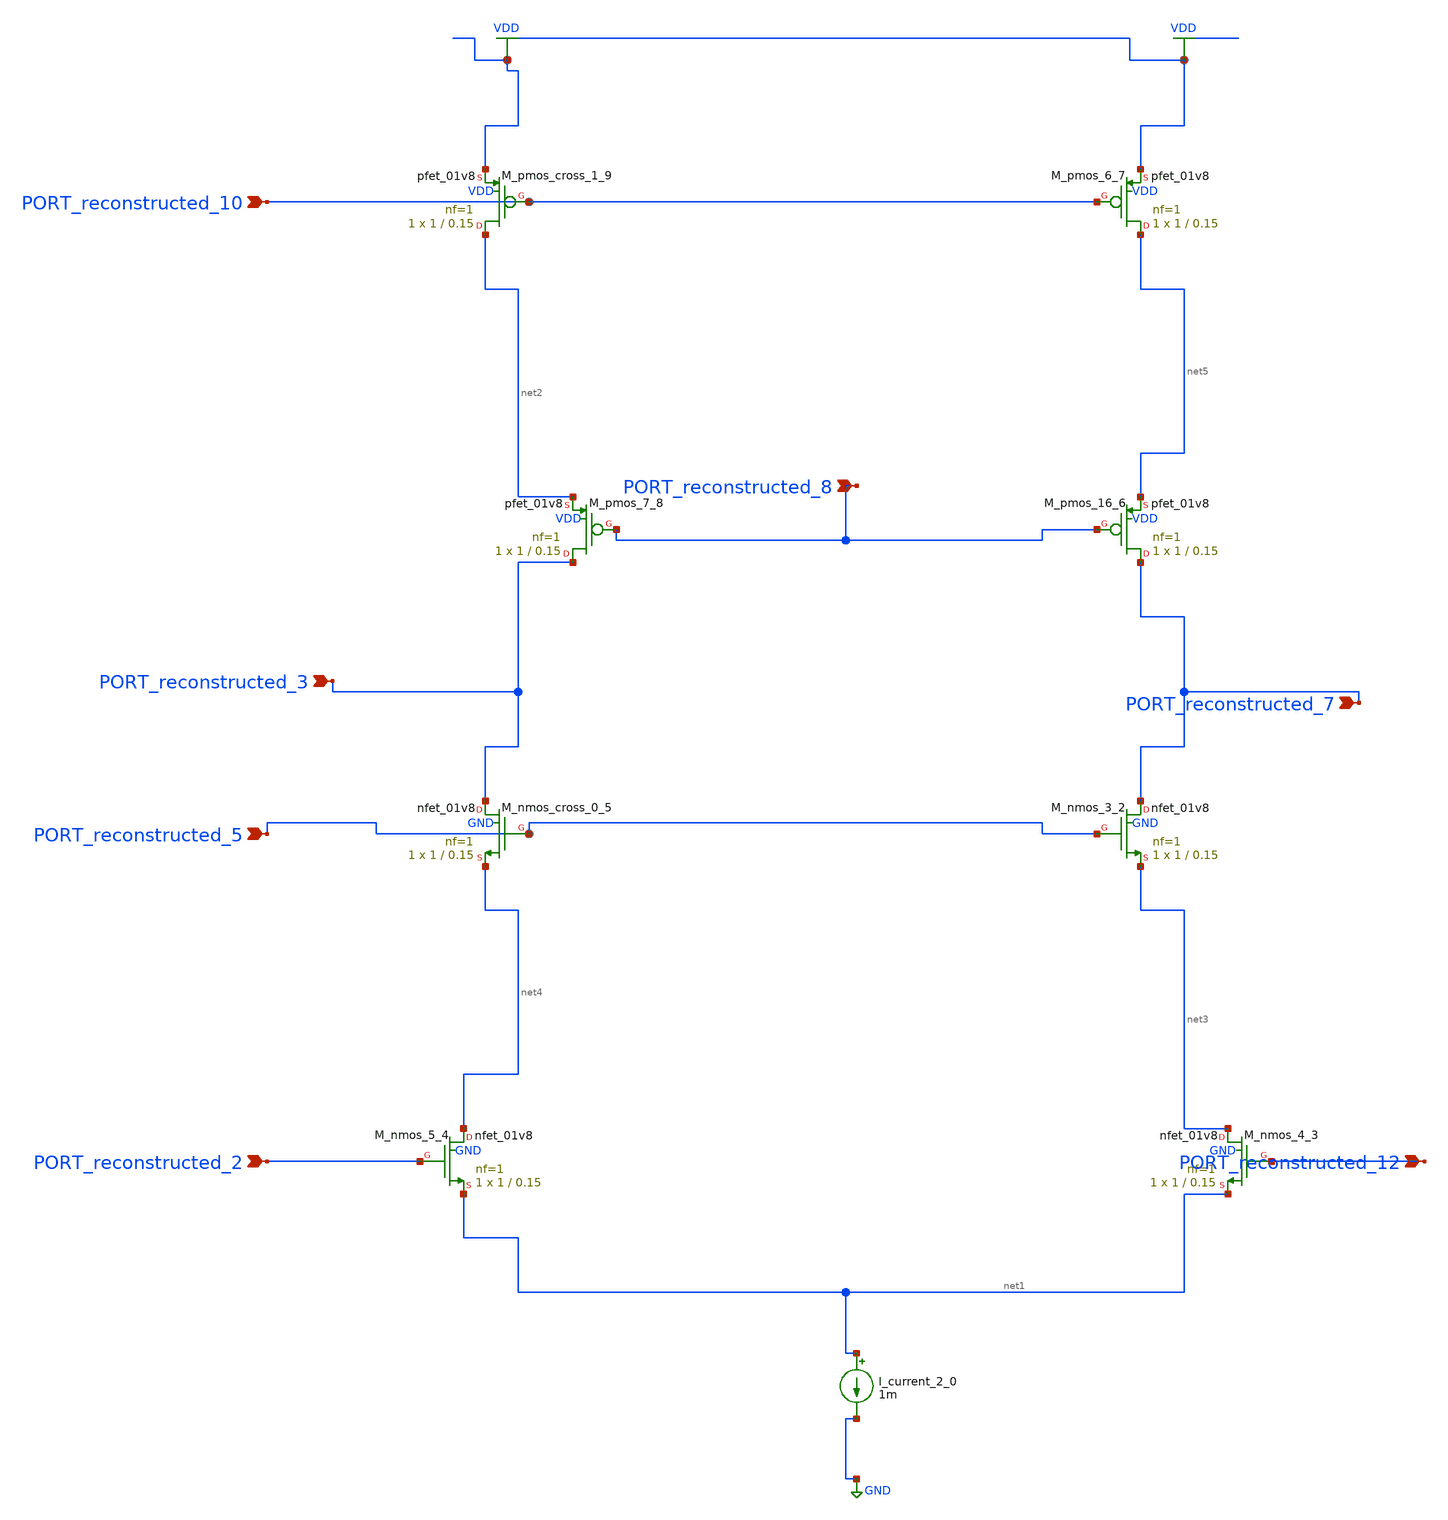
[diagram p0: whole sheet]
** sch_path: schematics/AMSNet/747.sch
**.subckt 747 PORT_reconstructed_5 PORT_reconstructed_3 PORT_reconstructed_7 PORT_reconstructed_12
*+ PORT_reconstructed_8 PORT_reconstructed_10 PORT_reconstructed_2
*.ipin PORT_reconstructed_5
*.ipin PORT_reconstructed_3
*.ipin PORT_reconstructed_7
*.ipin PORT_reconstructed_12
*.ipin PORT_reconstructed_8
*.ipin PORT_reconstructed_10
*.ipin PORT_reconstructed_2
I_current_2_0 net1 GND 1m
XM_nmos_3_2 PORT_reconstructed_7 PORT_reconstructed_5 net3 GND sky130_fd_pr__nfet_01v8 L=0.15 W=1 nf=1
+ ad='int((1 + 1)/2) * 1 / 1 * 0.29' as='int((1 + 2)/2) * 1 / 1 * 0.29' pd='2*int((1 + 1)/2) * (1 / 1 + 0.29)'
+ ps='2*int((1 + 2)/2) * (1 / 1 + 0.29)' nrd='0.29 / 1 ' nrs='0.29 / 1 ' sa=0 sb=0 sd=0 mult=1 m=1
XM_nmos_4_3 net3 PORT_reconstructed_12 net1 GND sky130_fd_pr__nfet_01v8 L=0.15 W=1 nf=1 ad='int((1 + 1)/2) * 1 / 1 * 0.29'
+ as='int((1 + 2)/2) * 1 / 1 * 0.29' pd='2*int((1 + 1)/2) * (1 / 1 + 0.29)' ps='2*int((1 + 2)/2) * (1 / 1 + 0.29)'
+ nrd='0.29 / 1 ' nrs='0.29 / 1 ' sa=0 sb=0 sd=0 mult=1 m=1
XM_nmos_5_4 net4 PORT_reconstructed_2 net1 GND sky130_fd_pr__nfet_01v8 L=0.15 W=1 nf=1 ad='int((1 + 1)/2) * 1 / 1 * 0.29'
+ as='int((1 + 2)/2) * 1 / 1 * 0.29' pd='2*int((1 + 1)/2) * (1 / 1 + 0.29)' ps='2*int((1 + 2)/2) * (1 / 1 + 0.29)'
+ nrd='0.29 / 1 ' nrs='0.29 / 1 ' sa=0 sb=0 sd=0 mult=1 m=1
XM_nmos_cross_0_5 PORT_reconstructed_3 PORT_reconstructed_5 net4 GND sky130_fd_pr__nfet_01v8 L=0.15 W=1
+ nf=1 ad='int((1 + 1)/2) * 1 / 1 * 0.29' as='int((1 + 2)/2) * 1 / 1 * 0.29' pd='2*int((1 + 1)/2) * (1 / 1 + 0.29)'
+ ps='2*int((1 + 2)/2) * (1 / 1 + 0.29)' nrd='0.29 / 1 ' nrs='0.29 / 1 ' sa=0 sb=0 sd=0 mult=1 m=1
XM_pmos_16_6 PORT_reconstructed_7 PORT_reconstructed_8 net5 VDD sky130_fd_pr__pfet_01v8 L=0.15 W=1 nf=1
+ ad='int((1 + 1)/2) * 1 / 1 * 0.29' as='int((1 + 2)/2) * 1 / 1 * 0.29' pd='2*int((1 + 1)/2) * (1 / 1 + 0.29)'
+ ps='2*int((1 + 2)/2) * (1 / 1 + 0.29)' nrd='0.29 / 1 ' nrs='0.29 / 1 ' sa=0 sb=0 sd=0 mult=1 m=1
XM_pmos_6_7 net5 PORT_reconstructed_10 VDD VDD sky130_fd_pr__pfet_01v8 L=0.15 W=1 nf=1 ad='int((1 + 1)/2) * 1 / 1 * 0.29'
+ as='int((1 + 2)/2) * 1 / 1 * 0.29' pd='2*int((1 + 1)/2) * (1 / 1 + 0.29)' ps='2*int((1 + 2)/2) * (1 / 1 + 0.29)'
+ nrd='0.29 / 1 ' nrs='0.29 / 1 ' sa=0 sb=0 sd=0 mult=1 m=1
XM_pmos_7_8 PORT_reconstructed_3 PORT_reconstructed_8 net2 VDD sky130_fd_pr__pfet_01v8 L=0.15 W=1 nf=1
+ ad='int((1 + 1)/2) * 1 / 1 * 0.29' as='int((1 + 2)/2) * 1 / 1 * 0.29' pd='2*int((1 + 1)/2) * (1 / 1 + 0.29)'
+ ps='2*int((1 + 2)/2) * (1 / 1 + 0.29)' nrd='0.29 / 1 ' nrs='0.29 / 1 ' sa=0 sb=0 sd=0 mult=1 m=1
XM_pmos_cross_1_9 net2 PORT_reconstructed_10 VDD VDD sky130_fd_pr__pfet_01v8 L=0.15 W=1 nf=1 ad='int((1 + 1)/2) * 1 / 1 * 0.29'
+ as='int((1 + 2)/2) * 1 / 1 * 0.29' pd='2*int((1 + 1)/2) * (1 / 1 + 0.29)' ps='2*int((1 + 2)/2) * (1 / 1 + 0.29)'
+ nrd='0.29 / 1 ' nrs='0.29 / 1 ' sa=0 sb=0 sd=0 mult=1 m=1
**.ends
.GLOBAL GND
.GLOBAL VDD
.end
